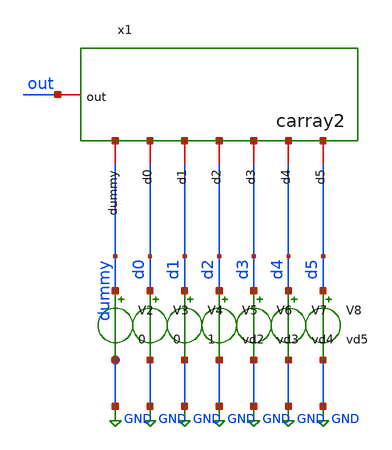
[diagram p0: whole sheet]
** sch_path: xschem/tb/cdac/tb_cdac.sch
**.subckt tb_cdac
x1 out d4 d1 d0 dummy d3 d2 d5 carray2
V2 dummy GND 0
V3 d0 GND 0
V4 d1 GND 1
V5 d2 GND vd2
V6 d3 GND vd3
V7 d4 GND vd4
V8 d5 GND vd5
**** begin user architecture code
 *.options method trap
*.options gmin 1e-15
*.options abstol 1e-15
*.options reltol 0.0001
*.options vntol 0.1e-6
*
*.include $::DESIGN_PATH/switches/bootstrapped_sw.sp


.param MC_SWITCH=0

*.tran 100e-9 4e-6
.temp 85

.control
save all
* tran 100e-9 13e-6 uic


*loop
.param vd0=0
.param vd1=1
.param vd2=1
.param vd3=1
.param vd4=1
.param vd5=1

op
dc V2 0 1 0.1
run


.endc

 * FET CORNERS
.include $::SKYWATER_MODELS/models/corners/tt.spice
*.include $::SKYWATER_MODELS//corners/ff.spice
*.include $::SKYWATER_MODELS/corners/ss.spice
*.include $::SKYWATER_MODELS/corners/sf.spice
*.include $::SKYWATER_MODELS/corners/fs.spice

* TT + R + C
*.include $::SKYWATER_MODELS/corners/tt_rmax_cmax.spice
*.include $::SKYWATER_MODELS/corners/tt_rmin_cmin.spice
*.include $::SKYWATER_MODELS/corners/tt_rmax_cmin.spice
*.include $::SKYWATER_MODELS/corners/tt_rmin_cmax.spice

* FF + R + C
*.include $::SKYWATER_MODELS/corners/ff_rmax_cmax.spice
*.include $::SKYWATER_MODELS/corners/ff_rmin_cmin.spice
*.include $::SKYWATER_MODELS/corners/ff_rmax_cmin.spice
*.include $::SKYWATER_MODELS/corners/ff_rmin_cmax.spice


* SS + R + C
*.include $::SKYWATER_MODELS/corners/ss_rmax_cmax.spice
*.include $::SKYWATER_MODELS/corners/ss_rmin_cmin.spice
*.include $::SKYWATER_MODELS/corners/ss_rmax_cmin.spice
*.include $::SKYWATER_MODELS/corners/ss_rmin_cmax.spice

* SF + R + C
*.include $::SKYWATER_MODELS/corners/sf_rmax_cmax.spice
*.include $::SKYWATER_MODELS/corners/sf_rmin_cmin.spice
*.include $::SKYWATER_MODELS/corners/sf_rmax_cmin.spice
*.include $::SKYWATER_MODELS/corners/sf_rmin_cmax.spice

* FS + R + C
*.include $::SKYWATER_MODELS/corners/fs_rmax_cmax.spice
*.include $::SKYWATER_MODELS/corners/fs_rmin_cmin.spice
*.include $::SKYWATER_MODELS/corners/fs_rmax_cmin.spice
*.include $::SKYWATER_MODELS/corners/fs_rmin_cmax.spice

**** end user architecture code
**.ends

* expanding   symbol:  sar_10b/dac/carray2.sym # of pins=8
** sym_path: xschem/sar_10b/dac/carray2.sym
** sch_path: xschem/sar_10b/dac/carray2.sch
.subckt carray2 out d4 d1 d0 dummy d3 d2 d5
*.iopin out
*.iopin d5
*.iopin d4
*.iopin d2
*.iopin d0
*.iopin dummy
*.iopin d3
*.iopin d1
C1 out dummy 2.6f m=1
C2 out d0 2.6f m=1
C3[1] out d1 2.6f m=1
C3[0] out d1 2.6f m=1
C4[3] out d2 2.6f m=1
C4[2] out d2 2.6f m=1
C4[1] out d2 2.6f m=1
C4[0] out d2 2.6f m=1
C5[7] out d3 2.6f m=1
C5[6] out d3 2.6f m=1
C5[5] out d3 2.6f m=1
C5[4] out d3 2.6f m=1
C5[3] out d3 2.6f m=1
C5[2] out d3 2.6f m=1
C5[1] out d3 2.6f m=1
C5[0] out d3 2.6f m=1
C6[15] out d4 2.6f m=1
C6[14] out d4 2.6f m=1
C6[13] out d4 2.6f m=1
C6[12] out d4 2.6f m=1
C6[11] out d4 2.6f m=1
C6[10] out d4 2.6f m=1
C6[9] out d4 2.6f m=1
C6[8] out d4 2.6f m=1
C6[7] out d4 2.6f m=1
C6[6] out d4 2.6f m=1
C6[5] out d4 2.6f m=1
C6[4] out d4 2.6f m=1
C6[3] out d4 2.6f m=1
C6[2] out d4 2.6f m=1
C6[1] out d4 2.6f m=1
C6[0] out d4 2.6f m=1
C7[31] out d5 2.6f m=1
C7[30] out d5 2.6f m=1
C7[29] out d5 2.6f m=1
C7[28] out d5 2.6f m=1
C7[27] out d5 2.6f m=1
C7[26] out d5 2.6f m=1
C7[25] out d5 2.6f m=1
C7[24] out d5 2.6f m=1
C7[23] out d5 2.6f m=1
C7[22] out d5 2.6f m=1
C7[21] out d5 2.6f m=1
C7[20] out d5 2.6f m=1
C7[19] out d5 2.6f m=1
C7[18] out d5 2.6f m=1
C7[17] out d5 2.6f m=1
C7[16] out d5 2.6f m=1
C7[15] out d5 2.6f m=1
C7[14] out d5 2.6f m=1
C7[13] out d5 2.6f m=1
C7[12] out d5 2.6f m=1
C7[11] out d5 2.6f m=1
C7[10] out d5 2.6f m=1
C7[9] out d5 2.6f m=1
C7[8] out d5 2.6f m=1
C7[7] out d5 2.6f m=1
C7[6] out d5 2.6f m=1
C7[5] out d5 2.6f m=1
C7[4] out d5 2.6f m=1
C7[3] out d5 2.6f m=1
C7[2] out d5 2.6f m=1
C7[1] out d5 2.6f m=1
C7[0] out d5 2.6f m=1
.ends

.GLOBAL GND
.end
